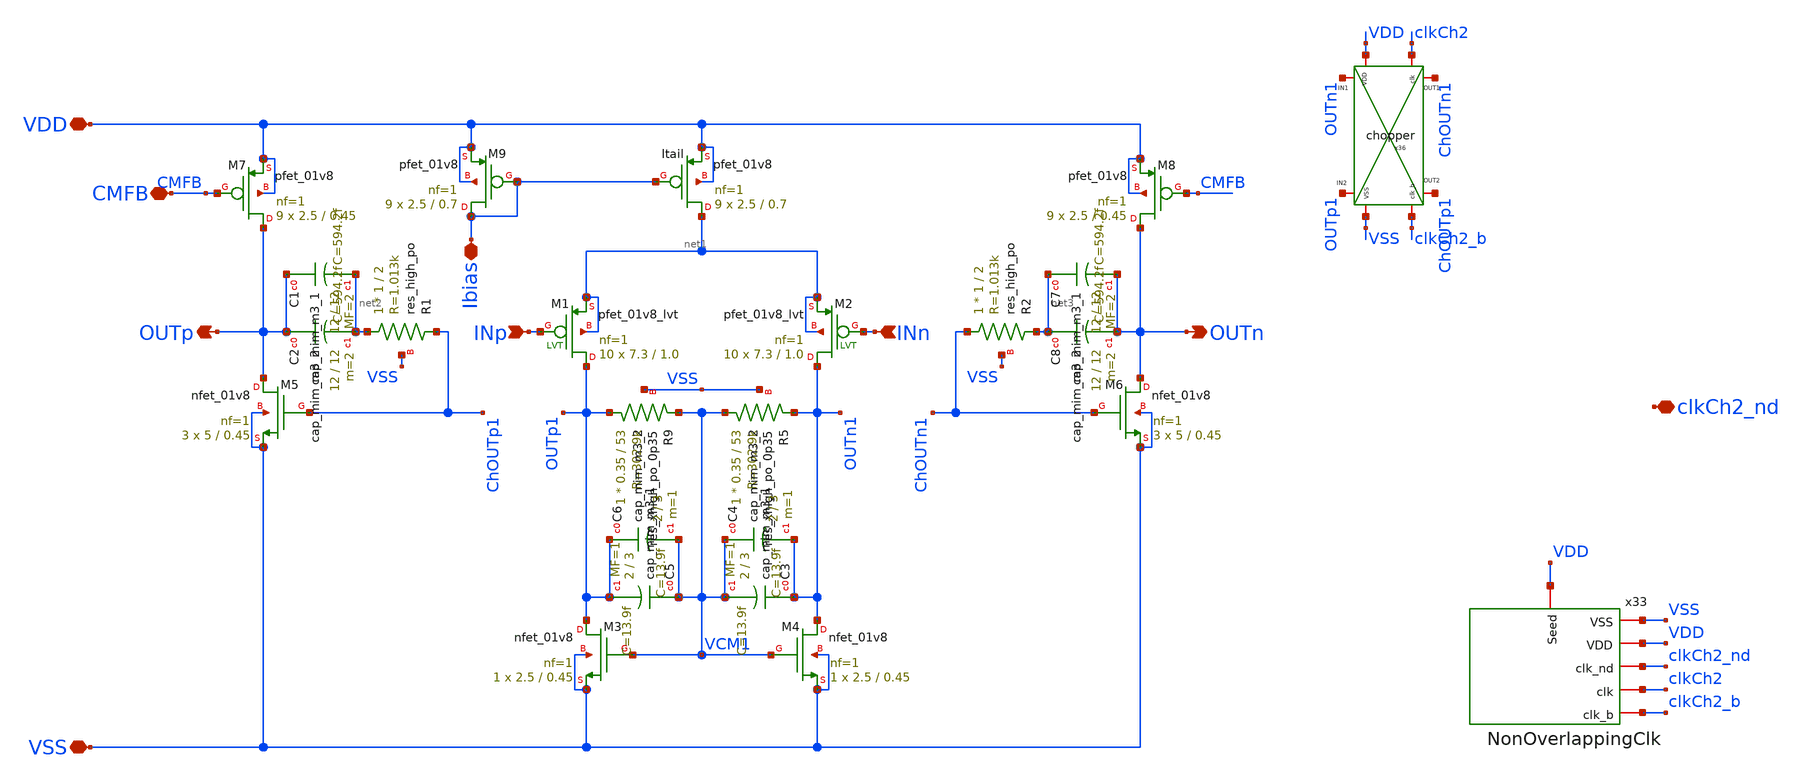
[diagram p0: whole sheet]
** sch_path: xschem/lib/Analog/FullyDiffOTA.sch
**.subckt FullyDiffOTA CMFB INp VDD INn VSS OUTp OUTn Ibias clkCh2_nd
*.iopin CMFB
*.ipin INp
*.iopin VDD
*.ipin INn
*.iopin VSS
*.opin OUTp
*.opin OUTn
*.iopin Ibias
*.iopin clkCh2_nd
XItail net1 Ibias VDD VDD sky130_fd_pr__pfet_01v8 L=0.7 W=2.5 nf=1 ad='int((nf+1)/2) * W/nf * 0.29' as='int((nf+2)/2) * W/nf * 0.29'
+ pd='2*int((nf+1)/2) * (W/nf + 0.29)' ps='2*int((nf+2)/2) * (W/nf + 0.29)' nrd='0.29 / W' nrs='0.29 / W'
+ sa=0 sb=0 sd=0 mult=9 m=9
XM1 OUTp1 INp net1 net1 sky130_fd_pr__pfet_01v8_lvt L=1.0 W=7.3 nf=1 ad='int((1 + 1)/2) * 7.3 / 1 * 0.29'
+ as='int((1 + 2)/2) * 7.3 / 1 * 0.29' pd='2*int((1 + 1)/2) * (7.3 / 1 + 0.29)' ps='2*int((1 + 2)/2) * (7.3 / 1 + 0.29)'
+ nrd='0.29 / 7.3 ' nrs='0.29 / 7.3 ' sa=0 sb=0 sd=0 mult=10 m=10
XM2 OUTn1 INn net1 net1 sky130_fd_pr__pfet_01v8_lvt L=1.0 W=7.3 nf=1 ad='int((1 + 1)/2) * 7.3 / 1 * 0.29'
+ as='int((1 + 2)/2) * 7.3 / 1 * 0.29' pd='2*int((1 + 1)/2) * (7.3 / 1 + 0.29)' ps='2*int((1 + 2)/2) * (7.3 / 1 + 0.29)'
+ nrd='0.29 / 7.3 ' nrs='0.29 / 7.3 ' sa=0 sb=0 sd=0 mult=10 m=10
XM3 OUTp1 VCM1 VSS VSS sky130_fd_pr__nfet_01v8 L=0.45 W=2.5 nf=1 ad='int((1 + 1)/2) * 2.5 / 1 * 0.29'
+ as='int((1 + 2)/2) * 2.5 / 1 * 0.29' pd='2*int((1 + 1)/2) * (2.5 / 1 + 0.29)' ps='2*int((1 + 2)/2) * (2.5 / 1 + 0.29)'
+ nrd='0.29 / 2.5 ' nrs='0.29 / 2.5 ' sa=0 sb=0 sd=0 mult=1 m=1
XM4 OUTn1 VCM1 VSS VSS sky130_fd_pr__nfet_01v8 L=0.45 W=2.5 nf=1 ad='int((1 + 1)/2) * 2.5 / 1 * 0.29'
+ as='int((1 + 2)/2) * 2.5 / 1 * 0.29' pd='2*int((1 + 1)/2) * (2.5 / 1 + 0.29)' ps='2*int((1 + 2)/2) * (2.5 / 1 + 0.29)'
+ nrd='0.29 / 2.5 ' nrs='0.29 / 2.5 ' sa=0 sb=0 sd=0 mult=1 m=1
XM5 OUTp ChOUTp1 VSS VSS sky130_fd_pr__nfet_01v8 L=0.45 W=5 nf=1 ad='int((1 + 1)/2) * 5 / 1 * 0.29' as='int((1 + 2)/2) * 5 / 1 * 0.29'
+ pd='2*int((1 + 1)/2) * (5 / 1 + 0.29)' ps='2*int((1 + 2)/2) * (5 / 1 + 0.29)' nrd='0.29 / 5 ' nrs='0.29 / 5 '
+ sa=0 sb=0 sd=0 mult=3 m=3
XM6 OUTn ChOUTn1 VSS VSS sky130_fd_pr__nfet_01v8 L=0.45 W=5 nf=1 ad='int((1 + 1)/2) * 5 / 1 * 0.29' as='int((1 + 2)/2) * 5 / 1 * 0.29'
+ pd='2*int((1 + 1)/2) * (5 / 1 + 0.29)' ps='2*int((1 + 2)/2) * (5 / 1 + 0.29)' nrd='0.29 / 5 ' nrs='0.29 / 5 '
+ sa=0 sb=0 sd=0 mult=3 m=3
XM7 OUTp CMFB VDD VDD sky130_fd_pr__pfet_01v8 L=0.45 W=2.5 nf=1 ad='int((1 + 1)/2) * 2.5 / 1 * 0.29'
+ as='int((1 + 2)/2) * 2.5 / 1 * 0.29' pd='2*int((1 + 1)/2) * (2.5 / 1 + 0.29)' ps='2*int((1 + 2)/2) * (2.5 / 1 + 0.29)'
+ nrd='0.29 / 2.5 ' nrs='0.29 / 2.5 ' sa=0 sb=0 sd=0 mult=9 m=9
XM8 OUTn CMFB VDD VDD sky130_fd_pr__pfet_01v8 L=0.45 W=2.5 nf=1 ad='int((1 + 1)/2) * 2.5 / 1 * 0.29'
+ as='int((1 + 2)/2) * 2.5 / 1 * 0.29' pd='2*int((1 + 1)/2) * (2.5 / 1 + 0.29)' ps='2*int((1 + 2)/2) * (2.5 / 1 + 0.29)'
+ nrd='0.29 / 2.5 ' nrs='0.29 / 2.5 ' sa=0 sb=0 sd=0 mult=9 m=9
XM9 Ibias Ibias VDD VDD sky130_fd_pr__pfet_01v8 L=0.7 W=2.5 nf=1 ad='int((nf+1)/2) * W/nf * 0.29' as='int((nf+2)/2) * W/nf * 0.29'
+ pd='2*int((nf+1)/2) * (W/nf + 0.29)' ps='2*int((nf+2)/2) * (W/nf + 0.29)' nrd='0.29 / W' nrs='0.29 / W'
+ sa=0 sb=0 sd=0 mult=9 m=9
XR9 OUTp1 VCM1 VSS sky130_fd_pr__res_xhigh_po_0p35 L=53 mult=1 m=1
XR5 VCM1 OUTn1 VSS sky130_fd_pr__res_xhigh_po_0p35 L=53 mult=1 m=1
XC5 VCM1 OUTp1 sky130_fd_pr__cap_mim_m3_1 W=2 L=3 MF=1 m=1
XC6 OUTp1 VCM1 sky130_fd_pr__cap_mim_m3_2 W=2 L=3 MF=1 m=1
XC3 OUTn1 VCM1 sky130_fd_pr__cap_mim_m3_1 W=2 L=3 MF=1 m=1
XC4 VCM1 OUTn1 sky130_fd_pr__cap_mim_m3_2 W=2 L=3 MF=1 m=1
XR1 net2 ChOUTp1 VSS sky130_fd_pr__res_high_po W=1 L=2 mult=1 m=1
XR2 ChOUTn1 net3 VSS sky130_fd_pr__res_high_po W=1 L=2 mult=1 m=1
XC7 net3 OUTn sky130_fd_pr__cap_mim_m3_1 W=12 L=12 MF=2 m=2
XC8 net3 OUTn sky130_fd_pr__cap_mim_m3_2 W=12 L=12 MF=2 m=2
XC1 OUTp net2 sky130_fd_pr__cap_mim_m3_1 W=12 L=12 MF=2 m=2
XC2 OUTp net2 sky130_fd_pr__cap_mim_m3_2 W=12 L=12 MF=2 m=2
x36 clkCh2 VDD clkCh2_b VSS ChOUTn1 OUTn1 ChOUTp1 OUTp1 chopper
x33 VSS VDD clkCh2_nd clkCh2 clkCh2_b VDD NonOverlappingClk
**.ends
.end
